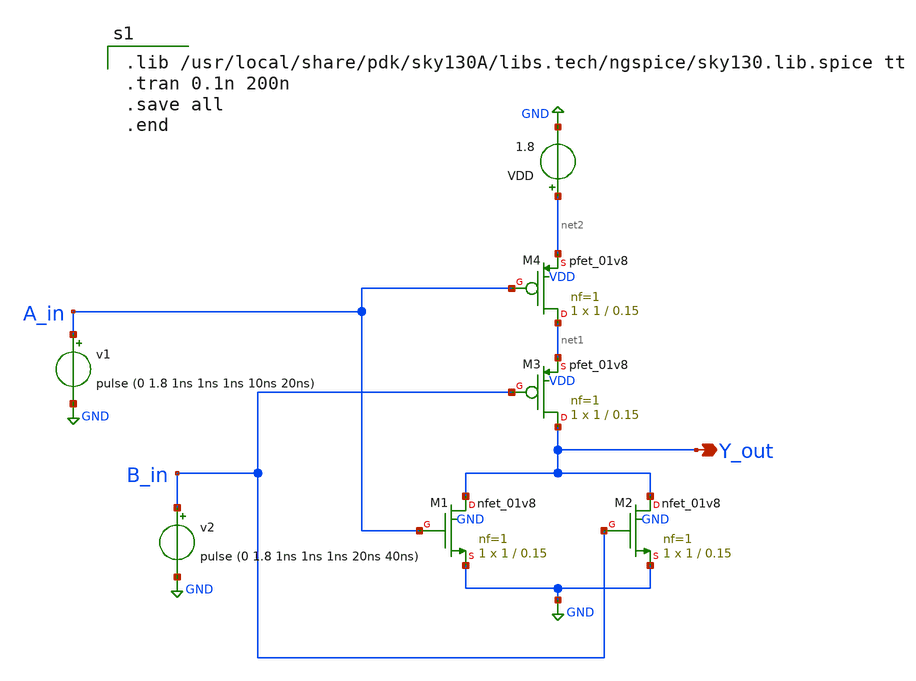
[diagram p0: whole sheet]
** sch_path: XSCHEM/nor/NOR.sch
**.subckt NOR Y_out
*.opin Y_out
XM1 Y_out A_in GND GND sky130_fd_pr__nfet_01v8 L=0.15 W=1 nf=1 ad='int((nf+1)/2) * W/nf * 0.29' as='int((nf+2)/2) * W/nf * 0.29'
+ pd='2*int((nf+1)/2) * (W/nf + 0.29)' ps='2*int((nf+2)/2) * (W/nf + 0.29)' nrd='0.29 / W' nrs='0.29 / W'
+ sa=0 sb=0 sd=0 mult=1 m=1
XM2 Y_out B_in GND GND sky130_fd_pr__nfet_01v8 L=0.15 W=1 nf=1 ad='int((nf+1)/2) * W/nf * 0.29' as='int((nf+2)/2) * W/nf * 0.29'
+ pd='2*int((nf+1)/2) * (W/nf + 0.29)' ps='2*int((nf+2)/2) * (W/nf + 0.29)' nrd='0.29 / W' nrs='0.29 / W'
+ sa=0 sb=0 sd=0 mult=1 m=1
XM3 Y_out B_in net1 VDD sky130_fd_pr__pfet_01v8 L=0.15 W=1 nf=1 ad='int((nf+1)/2) * W/nf * 0.29' as='int((nf+2)/2) * W/nf * 0.29'
+ pd='2*int((nf+1)/2) * (W/nf + 0.29)' ps='2*int((nf+2)/2) * (W/nf + 0.29)' nrd='0.29 / W' nrs='0.29 / W'
+ sa=0 sb=0 sd=0 mult=1 m=1
XM4 net1 A_in net2 VDD sky130_fd_pr__pfet_01v8 L=0.15 W=1 nf=1 ad='int((nf+1)/2) * W/nf * 0.29' as='int((nf+2)/2) * W/nf * 0.29'
+ pd='2*int((nf+1)/2) * (W/nf + 0.29)' ps='2*int((nf+2)/2) * (W/nf + 0.29)' nrd='0.29 / W' nrs='0.29 / W'
+ sa=0 sb=0 sd=0 mult=1 m=1
v1 A_in GND pulse (0 1.8 1ns 1ns 1ns 10ns 20ns)
v2 B_in GND pulse (0 1.8 1ns 1ns 1ns 20ns 40ns)
VDD net2 GND 1.8
**** begin user architecture code

.lib /usr/local/share/pdk/sky130A/libs.tech/ngspice/sky130.lib.spice tt
.tran 0.1n 200n
.save all
.end

**** end user architecture code
**.ends
.GLOBAL GND
.end
